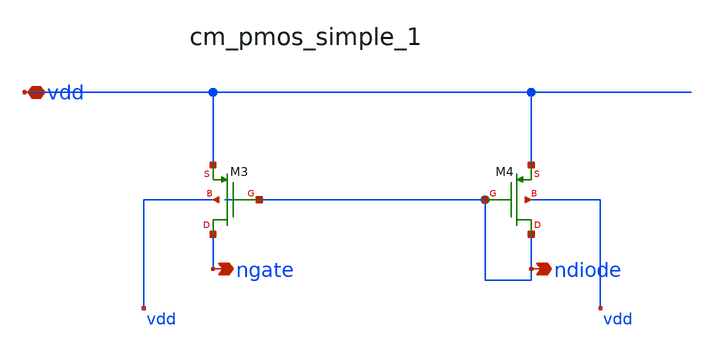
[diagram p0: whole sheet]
** sch_path: analog-db/raw/ldo_003_analoggym_simple/hier/blocks/cm_pmos_simple_1.sch
**.subckt cm_pmos_simple_1 vdd ndiode ngate
*.iopin vdd
*.opin ndiode
*.opin ngate
XM3 ngate ndiode vdd vdd sg13_hv_pmos w=x_dut_xm3_w l=x_dut_xm3_l ng=1 m=1
XM4 ndiode ndiode vdd vdd sg13_hv_pmos w=x_dut_xm4_w l=x_dut_xm4_l ng=1 m=1
**.ends
.end
